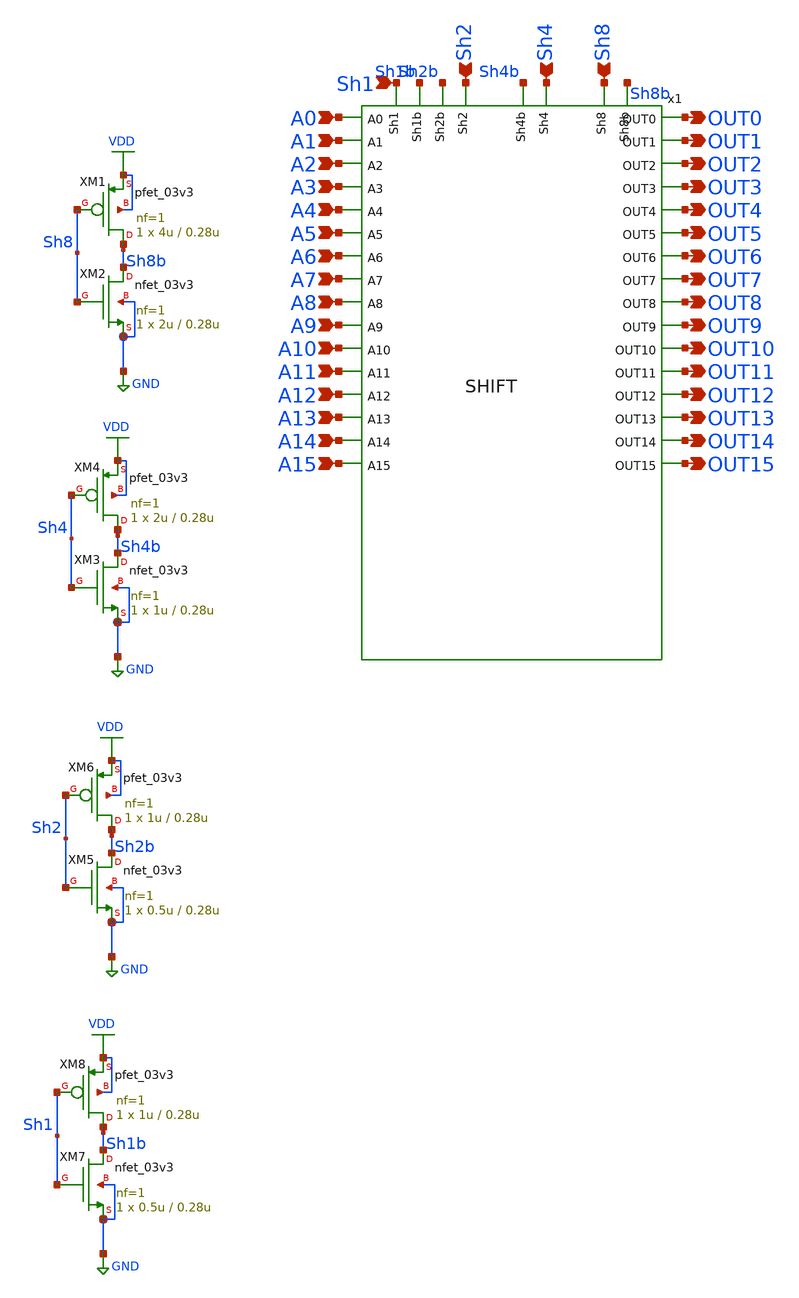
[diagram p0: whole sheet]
** sch_path: SHIFT_INVERTERS.sch
**.subckt SHIFT_INVERTERS OUT0 OUT1 OUT2 OUT3 OUT4 OUT5 OUT6 OUT7 OUT8 OUT9 OUT10 OUT11 OUT12 OUT13
*+ OUT14 OUT15 A0 A1 A2 A3 A4 A5 A6 A7 A8 A9 A10 A11 A12 A13 A14 A15 Sh1 Sh2 Sh4 Sh8
*.opin OUT0
*.opin OUT1
*.opin OUT2
*.opin OUT3
*.opin OUT4
*.opin OUT5
*.opin OUT6
*.opin OUT7
*.opin OUT8
*.opin OUT9
*.opin OUT10
*.opin OUT11
*.opin OUT12
*.opin OUT13
*.opin OUT14
*.opin OUT15
*.ipin A0
*.ipin A1
*.ipin A2
*.ipin A3
*.ipin A4
*.ipin A5
*.ipin A6
*.ipin A7
*.ipin A8
*.ipin A9
*.ipin A10
*.ipin A11
*.ipin A12
*.ipin A13
*.ipin A14
*.ipin A15
*.ipin Sh1
*.ipin Sh2
*.ipin Sh4
*.ipin Sh8
x1 Sh1b Sh1 Sh2 Sh2b A0 OUT0 A1 OUT1 Sh4 Sh4b A2 OUT2 A3 OUT3 Sh8b Sh8 OUT4 A4 OUT5 A5 OUT6 A6 OUT7
+ A7 OUT8 A8 A9 OUT9 A10 OUT10 OUT11 A11 OUT12 A12 A13 OUT13 OUT14 A14 OUT15 A15 SHIFT
XM2 Sh8b Sh8 GND GND nfet_03v3 L=0.28u W=2u nf=1 ad='int((nf+1)/2) * W/nf * 0.18u' as='int((nf+2)/2) * W/nf * 0.18u'
+ pd='2*int((nf+1)/2) * (W/nf + 0.18u)' ps='2*int((nf+2)/2) * (W/nf + 0.18u)' nrd='0.18u / W' nrs='0.18u / W'
+ sa=0 sb=0 sd=0 m=1
XM1 Sh8b Sh8 VDD VDD pfet_03v3 L=0.28u W=4u nf=1 ad='int((nf+1)/2) * W/nf * 0.18u' as='int((nf+2)/2) * W/nf * 0.18u'
+ pd='2*int((nf+1)/2) * (W/nf + 0.18u)' ps='2*int((nf+2)/2) * (W/nf + 0.18u)' nrd='0.18u / W' nrs='0.18u / W'
+ sa=0 sb=0 sd=0 m=1
XM3 Sh4b Sh4 GND GND nfet_03v3 L=0.28u W=1u nf=1 ad='int((nf+1)/2) * W/nf * 0.18u' as='int((nf+2)/2) * W/nf * 0.18u'
+ pd='2*int((nf+1)/2) * (W/nf + 0.18u)' ps='2*int((nf+2)/2) * (W/nf + 0.18u)' nrd='0.18u / W' nrs='0.18u / W'
+ sa=0 sb=0 sd=0 m=1
XM4 Sh4b Sh4 VDD VDD pfet_03v3 L=0.28u W=2u nf=1 ad='int((nf+1)/2) * W/nf * 0.18u' as='int((nf+2)/2) * W/nf * 0.18u'
+ pd='2*int((nf+1)/2) * (W/nf + 0.18u)' ps='2*int((nf+2)/2) * (W/nf + 0.18u)' nrd='0.18u / W' nrs='0.18u / W'
+ sa=0 sb=0 sd=0 m=1
XM5 Sh2b Sh2 GND GND nfet_03v3 L=0.28u W=0.5u nf=1 ad='int((nf+1)/2) * W/nf * 0.18u' as='int((nf+2)/2) * W/nf * 0.18u'
+ pd='2*int((nf+1)/2) * (W/nf + 0.18u)' ps='2*int((nf+2)/2) * (W/nf + 0.18u)' nrd='0.18u / W' nrs='0.18u / W'
+ sa=0 sb=0 sd=0 m=1
XM6 Sh2b Sh2 VDD VDD pfet_03v3 L=0.28u W=1u nf=1 ad='int((nf+1)/2) * W/nf * 0.18u' as='int((nf+2)/2) * W/nf * 0.18u'
+ pd='2*int((nf+1)/2) * (W/nf + 0.18u)' ps='2*int((nf+2)/2) * (W/nf + 0.18u)' nrd='0.18u / W' nrs='0.18u / W'
+ sa=0 sb=0 sd=0 m=1
XM7 Sh1b Sh1 GND GND nfet_03v3 L=0.28u W=0.5u nf=1 ad='int((nf+1)/2) * W/nf * 0.18u' as='int((nf+2)/2) * W/nf * 0.18u'
+ pd='2*int((nf+1)/2) * (W/nf + 0.18u)' ps='2*int((nf+2)/2) * (W/nf + 0.18u)' nrd='0.18u / W' nrs='0.18u / W'
+ sa=0 sb=0 sd=0 m=1
XM8 Sh1b Sh1 VDD VDD pfet_03v3 L=0.28u W=1u nf=1 ad='int((nf+1)/2) * W/nf * 0.18u' as='int((nf+2)/2) * W/nf * 0.18u'
+ pd='2*int((nf+1)/2) * (W/nf + 0.18u)' ps='2*int((nf+2)/2) * (W/nf + 0.18u)' nrd='0.18u / W' nrs='0.18u / W'
+ sa=0 sb=0 sd=0 m=1
**.ends
.GLOBAL GND
.GLOBAL VDD
.end
